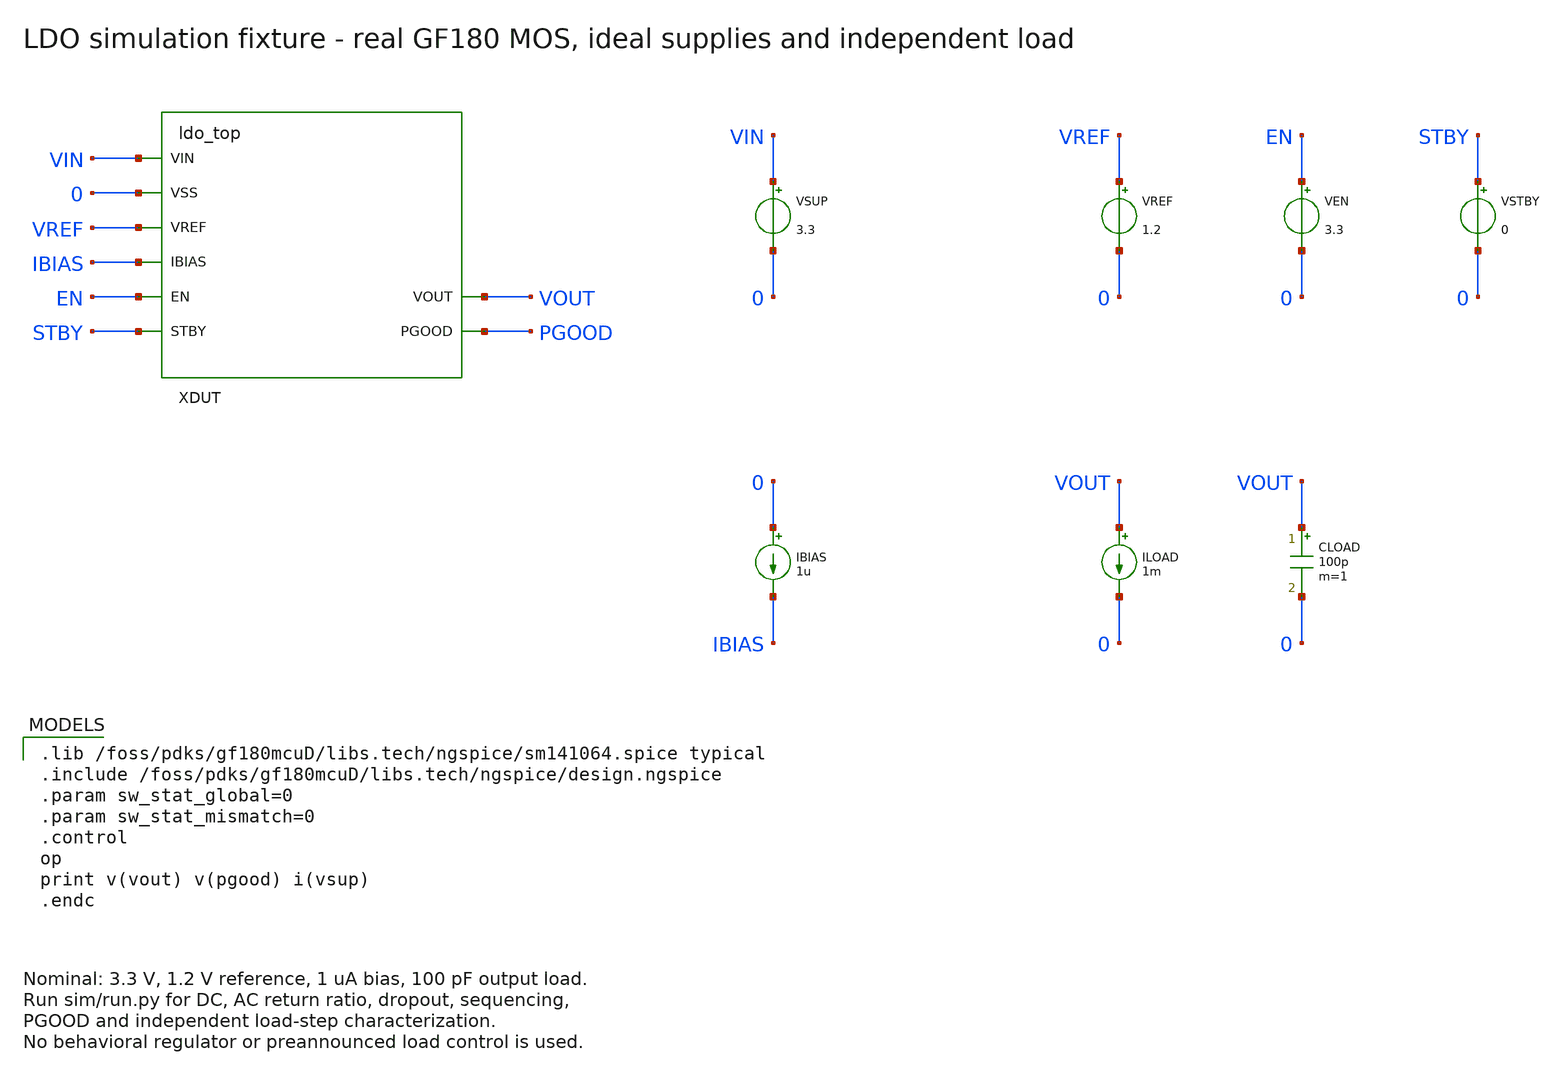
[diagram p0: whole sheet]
** sch_path: schematics/ldo_tb.sch
**.subckt ldo_tb
XDUT VIN 0 VREF IBIAS EN STBY VOUT PGOOD ldo_top
VSUP VIN 0 3.3
VREF VREF 0 1.2
VEN EN 0 3.3
VSTBY STBY 0 0
IBIAS 0 IBIAS 1u
ILOAD VOUT 0 1m
CLOAD VOUT 0 100p m=1
**** begin user architecture code

.lib /foss/pdks/gf180mcuD/libs.tech/ngspice/sm141064.spice typical
.include /foss/pdks/gf180mcuD/libs.tech/ngspice/design.ngspice
.param sw_stat_global=0
.param sw_stat_mismatch=0
.control
op
print v(vout) v(pgood) i(vsup)
.endc

**** end user architecture code
**.ends

* expanding   symbol:  ldo_top.sym # of pins=8
** sym_path: schematics/ldo_top.sym
** sch_path: schematics/ldo_top.sch
.subckt ldo_top VIN VSS VREF IBIAS EN STBY VOUT PGOOD
*.iopin VIN
*.iopin VSS
*.iopin VREF
*.iopin IBIAS
*.iopin EN
*.iopin STBY
*.iopin VOUT
*.iopin PGOOD
XSS VSS ENB VREF VREF_SS ldo_softstart
XEA VIN VSS PB ENB VREF_SS VFB GATE ldo_error_amp
XPWR VIN VSS EN ENB GATE VOUT ldo_power_stage
XBIAS VIN VSS IBIAS EN STBY GATE ENB PB ldo_bias
XPG VIN VSS PB EN ENB VREF VFB PGOOD ldo_pgood
RTOP VOUT VFB 600k m=1
RBOT VFB VSS 1.2Meg m=1
RZERO GATE COMP 5k m=1
CC COMP VOUT 200p m=1
RBLEED VOUT VSS 360k m=1
.ends


* expanding   symbol:  ldo_softstart.sym # of pins=4
** sym_path: schematics/ldo_softstart.sym
** sch_path: schematics/ldo_softstart.sch
.subckt ldo_softstart VSS ENB VREF VREF_SS
*.iopin VSS
*.iopin ENB
*.iopin VREF
*.iopin VREF_SS
RSS VREF VREF_SS 1Meg m=1
CSS VREF_SS VSS 20p m=1
XMNRESET VREF_SS ENB VSS VSS nfet_03v3 L=0.5u W=2u nf=1 ad='int((nf+1)/2)*W/nf*0.18u' as='int((nf+2)/2)*W/nf*0.18u'
+ pd='2*int((nf+1)/2)*(W/nf+0.18u)' ps='2*int((nf+2)/2)*(W/nf+0.18u)' nrd='0.18u/W' nrs='0.18u/W' sa=0
+ sb=0 sd=0 m=1 par=1
.ends


* expanding   symbol:  ldo_error_amp.sym # of pins=7
** sym_path: schematics/ldo_error_amp.sym
** sch_path: schematics/ldo_error_amp.sch
.subckt ldo_error_amp VIN VSS PB ENB VREF VFB GATE
*.iopin VIN
*.iopin VSS
*.iopin PB
*.iopin ENB
*.iopin VREF
*.iopin VFB
*.iopin GATE
XMPEN VP ENB VIN VIN pfet_03v3 L=0.5u W=20u nf=1 ad='int((nf+1)/2)*W/nf*0.18u' as='int((nf+2)/2)*W/nf*0.18u'
+ pd='2*int((nf+1)/2)*(W/nf+0.18u)' ps='2*int((nf+2)/2)*(W/nf+0.18u)' nrd='0.18u/W' nrs='0.18u/W' sa=0
+ sb=0 sd=0 m=1 par=1
XMPBIAS NB PB VP VIN pfet_03v3 L=2u W=4u nf=1 ad='int((nf+1)/2)*W/nf*0.18u' as='int((nf+2)/2)*W/nf*0.18u'
+ pd='2*int((nf+1)/2)*(W/nf+0.18u)' ps='2*int((nf+2)/2)*(W/nf+0.18u)' nrd='0.18u/W' nrs='0.18u/W' sa=0
+ sb=0 sd=0 m=1 par=1
XMNBIAS NB NB VSS VSS nfet_03v3 L=2u W=2u nf=1 ad='int((nf+1)/2)*W/nf*0.18u' as='int((nf+2)/2)*W/nf*0.18u'
+ pd='2*int((nf+1)/2)*(W/nf+0.18u)' ps='2*int((nf+2)/2)*(W/nf+0.18u)' nrd='0.18u/W' nrs='0.18u/W' sa=0
+ sb=0 sd=0 m=1 par=1
XMPMIR MIR MIR VP VIN pfet_03v3 L=2u W=8u nf=1 ad='int((nf+1)/2)*W/nf*0.18u' as='int((nf+2)/2)*W/nf*0.18u'
+ pd='2*int((nf+1)/2)*(W/nf+0.18u)' ps='2*int((nf+2)/2)*(W/nf+0.18u)' nrd='0.18u/W' nrs='0.18u/W' sa=0
+ sb=0 sd=0 m=1 par=1
XMPOUT EA MIR VP VIN pfet_03v3 L=2u W=8u nf=1 ad='int((nf+1)/2)*W/nf*0.18u' as='int((nf+2)/2)*W/nf*0.18u'
+ pd='2*int((nf+1)/2)*(W/nf+0.18u)' ps='2*int((nf+2)/2)*(W/nf+0.18u)' nrd='0.18u/W' nrs='0.18u/W' sa=0
+ sb=0 sd=0 m=1 par=1
XMNREF MIR VREF TAIL VSS nfet_03v3 L=1u W=20u nf=1 ad='int((nf+1)/2)*W/nf*0.18u' as='int((nf+2)/2)*W/nf*0.18u'
+ pd='2*int((nf+1)/2)*(W/nf+0.18u)' ps='2*int((nf+2)/2)*(W/nf+0.18u)' nrd='0.18u/W' nrs='0.18u/W' sa=0
+ sb=0 sd=0 m=1 par=1
XMNFB EA VFB TAIL VSS nfet_03v3 L=1u W=20u nf=1 ad='int((nf+1)/2)*W/nf*0.18u' as='int((nf+2)/2)*W/nf*0.18u'
+ pd='2*int((nf+1)/2)*(W/nf+0.18u)' ps='2*int((nf+2)/2)*(W/nf+0.18u)' nrd='0.18u/W' nrs='0.18u/W' sa=0
+ sb=0 sd=0 m=1 par=1
XMNTAIL TAIL NB VSS VSS nfet_03v3 L=2u W=4u nf=1 ad='int((nf+1)/2)*W/nf*0.18u' as='int((nf+2)/2)*W/nf*0.18u'
+ pd='2*int((nf+1)/2)*(W/nf+0.18u)' ps='2*int((nf+2)/2)*(W/nf+0.18u)' nrd='0.18u/W' nrs='0.18u/W' sa=0
+ sb=0 sd=0 m=1 par=1
XMPDRV GATE PB VP VIN pfet_03v3 L=2u W=16u nf=1 ad='int((nf+1)/2)*W/nf*0.18u' as='int((nf+2)/2)*W/nf*0.18u'
+ pd='2*int((nf+1)/2)*(W/nf+0.18u)' ps='2*int((nf+2)/2)*(W/nf+0.18u)' nrd='0.18u/W' nrs='0.18u/W' sa=0
+ sb=0 sd=0 m=1 par=1
XMNDRV GATE EA VSS VSS nfet_03v3 L=4u W=2u nf=1 ad='int((nf+1)/2)*W/nf*0.18u' as='int((nf+2)/2)*W/nf*0.18u'
+ pd='2*int((nf+1)/2)*(W/nf+0.18u)' ps='2*int((nf+2)/2)*(W/nf+0.18u)' nrd='0.18u/W' nrs='0.18u/W' sa=0
+ sb=0 sd=0 m=1 par=1
XMNCLAMP EA ENB VSS VSS nfet_03v3 L=0.5u W=2u nf=1 ad='int((nf+1)/2)*W/nf*0.18u' as='int((nf+2)/2)*W/nf*0.18u'
+ pd='2*int((nf+1)/2)*(W/nf+0.18u)' ps='2*int((nf+2)/2)*(W/nf+0.18u)' nrd='0.18u/W' nrs='0.18u/W' sa=0
+ sb=0 sd=0 m=1 par=1
RZ EA CZ 330k m=1
CM CZ GATE 200p m=1
.ends


* expanding   symbol:  ldo_power_stage.sym # of pins=6
** sym_path: schematics/ldo_power_stage.sym
** sch_path: schematics/ldo_power_stage.sch
.subckt ldo_power_stage VIN VSS EN ENB GATE VOUT
*.iopin VIN
*.iopin VSS
*.iopin EN
*.iopin ENB
*.iopin GATE
*.iopin VOUT
XMPASS VOUT GATE VIN VIN pfet_03v3 L=0.28u W=50u nf=1 ad='int((nf+1)/2)*W/nf*0.18u' as='int((nf+2)/2)*W/nf*0.18u'
+ pd='2*int((nf+1)/2)*(W/nf+0.18u)' ps='2*int((nf+2)/2)*(W/nf+0.18u)' nrd='0.18u/W' nrs='0.18u/W' sa=0
+ sb=0 sd=0 m=200 par=200
XMPOFF GATE EN VIN VIN pfet_03v3 L=0.5u W=4u nf=1 ad='int((nf+1)/2)*W/nf*0.18u' as='int((nf+2)/2)*W/nf*0.18u'
+ pd='2*int((nf+1)/2)*(W/nf+0.18u)' ps='2*int((nf+2)/2)*(W/nf+0.18u)' nrd='0.18u/W' nrs='0.18u/W' sa=0
+ sb=0 sd=0 m=1 par=1
RDIS VOUT DIS 2k m=1
XMNDIS DIS ENB VSS VSS nfet_03v3 L=0.5u W=4u nf=1 ad='int((nf+1)/2)*W/nf*0.18u' as='int((nf+2)/2)*W/nf*0.18u'
+ pd='2*int((nf+1)/2)*(W/nf+0.18u)' ps='2*int((nf+2)/2)*(W/nf+0.18u)' nrd='0.18u/W' nrs='0.18u/W' sa=0
+ sb=0 sd=0 m=1 par=1
.ends


* expanding   symbol:  ldo_bias.sym # of pins=8
** sym_path: schematics/ldo_bias.sym
** sch_path: schematics/ldo_bias.sch
.subckt ldo_bias VIN VSS IBIAS EN STBY GATE ENB PB
*.iopin VIN
*.iopin VSS
*.iopin IBIAS
*.iopin EN
*.iopin STBY
*.iopin GATE
*.iopin ENB
*.iopin PB
XMNREF IBIAS IBIAS VSS VSS nfet_03v3 L=2u W=2u nf=1 ad='int((nf+1)/2)*W/nf*0.18u' as='int((nf+2)/2)*W/nf*0.18u'
+ pd='2*int((nf+1)/2)*(W/nf+0.18u)' ps='2*int((nf+2)/2)*(W/nf+0.18u)' nrd='0.18u/W' nrs='0.18u/W' sa=0
+ sb=0 sd=0 m=1 par=1
XMNCOPY PB IBIAS VSS VSS nfet_03v3 L=2u W=2u nf=1 ad='int((nf+1)/2)*W/nf*0.18u' as='int((nf+2)/2)*W/nf*0.18u'
+ pd='2*int((nf+1)/2)*(W/nf+0.18u)' ps='2*int((nf+2)/2)*(W/nf+0.18u)' nrd='0.18u/W' nrs='0.18u/W' sa=0
+ sb=0 sd=0 m=1 par=1
XMPREF PB PB VIN VIN pfet_03v3 L=2u W=4u nf=1 ad='int((nf+1)/2)*W/nf*0.18u' as='int((nf+2)/2)*W/nf*0.18u'
+ pd='2*int((nf+1)/2)*(W/nf+0.18u)' ps='2*int((nf+2)/2)*(W/nf+0.18u)' nrd='0.18u/W' nrs='0.18u/W' sa=0
+ sb=0 sd=0 m=1 par=1
XMPADEN ADSUP ENB VIN VIN pfet_03v3 L=0.5u W=4u nf=1 ad='int((nf+1)/2)*W/nf*0.18u' as='int((nf+2)/2)*W/nf*0.18u'
+ pd='2*int((nf+1)/2)*(W/nf+0.18u)' ps='2*int((nf+2)/2)*(W/nf+0.18u)' nrd='0.18u/W' nrs='0.18u/W' sa=0
+ sb=0 sd=0 m=1 par=1
XMPADMODE ADSOURCE STBY ADSUP VIN pfet_03v3 L=0.5u W=4u nf=1 ad='int((nf+1)/2)*W/nf*0.18u' as='int((nf+2)/2)*W/nf*0.18u'
+ pd='2*int((nf+1)/2)*(W/nf+0.18u)' ps='2*int((nf+2)/2)*(W/nf+0.18u)' nrd='0.18u/W' nrs='0.18u/W' sa=0
+ sb=0 sd=0 m=1 par=1
XMPREPLICA IBIAS GATE ADSOURCE VIN pfet_03v3 L=0.28u W=0.22u nf=1 ad='int((nf+1)/2)*W/nf*0.18u' as='int((nf+2)/2)*W/nf*0.18u'
+ pd='2*int((nf+1)/2)*(W/nf+0.18u)' ps='2*int((nf+2)/2)*(W/nf+0.18u)' nrd='0.18u/W' nrs='0.18u/W' sa=0
+ sb=0 sd=0 m=1 par=1
XMPINV ENB EN VIN VIN pfet_03v3 L=0.5u W=2u nf=1 ad='int((nf+1)/2)*W/nf*0.18u' as='int((nf+2)/2)*W/nf*0.18u'
+ pd='2*int((nf+1)/2)*(W/nf+0.18u)' ps='2*int((nf+2)/2)*(W/nf+0.18u)' nrd='0.18u/W' nrs='0.18u/W' sa=0
+ sb=0 sd=0 m=1 par=1
XMNINV ENB EN VSS VSS nfet_03v3 L=0.5u W=1u nf=1 ad='int((nf+1)/2)*W/nf*0.18u' as='int((nf+2)/2)*W/nf*0.18u'
+ pd='2*int((nf+1)/2)*(W/nf+0.18u)' ps='2*int((nf+2)/2)*(W/nf+0.18u)' nrd='0.18u/W' nrs='0.18u/W' sa=0
+ sb=0 sd=0 m=1 par=1
.ends


* expanding   symbol:  ldo_pgood.sym # of pins=8
** sym_path: schematics/ldo_pgood.sym
** sch_path: schematics/ldo_pgood.sch
.subckt ldo_pgood VIN VSS PB EN ENB VREF VFB PGOOD
*.iopin VIN
*.iopin VSS
*.iopin PB
*.iopin EN
*.iopin ENB
*.iopin VREF
*.iopin VFB
*.iopin PGOOD
XMPEN VP ENB VIN VIN pfet_03v3 L=0.5u W=8u nf=1 ad='int((nf+1)/2)*W/nf*0.18u' as='int((nf+2)/2)*W/nf*0.18u'
+ pd='2*int((nf+1)/2)*(W/nf+0.18u)' ps='2*int((nf+2)/2)*(W/nf+0.18u)' nrd='0.18u/W' nrs='0.18u/W' sa=0
+ sb=0 sd=0 m=1 par=1
XMPBIAS NB PB VP VIN pfet_03v3 L=2u W=2u nf=1 ad='int((nf+1)/2)*W/nf*0.18u' as='int((nf+2)/2)*W/nf*0.18u'
+ pd='2*int((nf+1)/2)*(W/nf+0.18u)' ps='2*int((nf+2)/2)*(W/nf+0.18u)' nrd='0.18u/W' nrs='0.18u/W' sa=0
+ sb=0 sd=0 m=1 par=1
XMNBIAS NB NB VSS VSS nfet_03v3 L=2u W=2u nf=1 ad='int((nf+1)/2)*W/nf*0.18u' as='int((nf+2)/2)*W/nf*0.18u'
+ pd='2*int((nf+1)/2)*(W/nf+0.18u)' ps='2*int((nf+2)/2)*(W/nf+0.18u)' nrd='0.18u/W' nrs='0.18u/W' sa=0
+ sb=0 sd=0 m=1 par=1
XMPMIR MIR MIR VP VIN pfet_03v3 L=2u W=4u nf=1 ad='int((nf+1)/2)*W/nf*0.18u' as='int((nf+2)/2)*W/nf*0.18u'
+ pd='2*int((nf+1)/2)*(W/nf+0.18u)' ps='2*int((nf+2)/2)*(W/nf+0.18u)' nrd='0.18u/W' nrs='0.18u/W' sa=0
+ sb=0 sd=0 m=1 par=1
XMPOUT RAW MIR VP VIN pfet_03v3 L=2u W=4u nf=1 ad='int((nf+1)/2)*W/nf*0.18u' as='int((nf+2)/2)*W/nf*0.18u'
+ pd='2*int((nf+1)/2)*(W/nf+0.18u)' ps='2*int((nf+2)/2)*(W/nf+0.18u)' nrd='0.18u/W' nrs='0.18u/W' sa=0
+ sb=0 sd=0 m=1 par=1
XMNREF MIR THRESH TAIL VSS nfet_03v3 L=1u W=8u nf=1 ad='int((nf+1)/2)*W/nf*0.18u' as='int((nf+2)/2)*W/nf*0.18u'
+ pd='2*int((nf+1)/2)*(W/nf+0.18u)' ps='2*int((nf+2)/2)*(W/nf+0.18u)' nrd='0.18u/W' nrs='0.18u/W' sa=0
+ sb=0 sd=0 m=1 par=1
XMNFB RAW VFB TAIL VSS nfet_03v3 L=1u W=8u nf=1 ad='int((nf+1)/2)*W/nf*0.18u' as='int((nf+2)/2)*W/nf*0.18u'
+ pd='2*int((nf+1)/2)*(W/nf+0.18u)' ps='2*int((nf+2)/2)*(W/nf+0.18u)' nrd='0.18u/W' nrs='0.18u/W' sa=0
+ sb=0 sd=0 m=1 par=1
XMNTAIL TAIL NB VSS VSS nfet_03v3 L=2u W=2u nf=1 ad='int((nf+1)/2)*W/nf*0.18u' as='int((nf+2)/2)*W/nf*0.18u'
+ pd='2*int((nf+1)/2)*(W/nf+0.18u)' ps='2*int((nf+2)/2)*(W/nf+0.18u)' nrd='0.18u/W' nrs='0.18u/W' sa=0
+ sb=0 sd=0 m=1 par=1
XMPBUF PGOOD RAW VIN VIN pfet_03v3 L=0.5u W=2u nf=1 ad='int((nf+1)/2)*W/nf*0.18u' as='int((nf+2)/2)*W/nf*0.18u'
+ pd='2*int((nf+1)/2)*(W/nf+0.18u)' ps='2*int((nf+2)/2)*(W/nf+0.18u)' nrd='0.18u/W' nrs='0.18u/W' sa=0
+ sb=0 sd=0 m=1 par=1
XMNBUF PGOOD RAW VSS VSS nfet_03v3 L=0.5u W=1u nf=1 ad='int((nf+1)/2)*W/nf*0.18u' as='int((nf+2)/2)*W/nf*0.18u'
+ pd='2*int((nf+1)/2)*(W/nf+0.18u)' ps='2*int((nf+2)/2)*(W/nf+0.18u)' nrd='0.18u/W' nrs='0.18u/W' sa=0
+ sb=0 sd=0 m=1 par=1
XMPOFF RAW EN VIN VIN pfet_03v3 L=0.5u W=2u nf=1 ad='int((nf+1)/2)*W/nf*0.18u' as='int((nf+2)/2)*W/nf*0.18u'
+ pd='2*int((nf+1)/2)*(W/nf+0.18u)' ps='2*int((nf+2)/2)*(W/nf+0.18u)' nrd='0.18u/W' nrs='0.18u/W' sa=0
+ sb=0 sd=0 m=1 par=1
RTH VREF THRESH 200k m=1
RLOW THRESH VSS 1.8Meg m=1
RHYS THRESH HYS 3.06Meg m=1
XMNHYS HYS PGOOD VSS VSS nfet_03v3 L=0.5u W=2u nf=1 ad='int((nf+1)/2)*W/nf*0.18u' as='int((nf+2)/2)*W/nf*0.18u'
+ pd='2*int((nf+1)/2)*(W/nf+0.18u)' ps='2*int((nf+2)/2)*(W/nf+0.18u)' nrd='0.18u/W' nrs='0.18u/W' sa=0
+ sb=0 sd=0 m=1 par=1
.ends

.end
